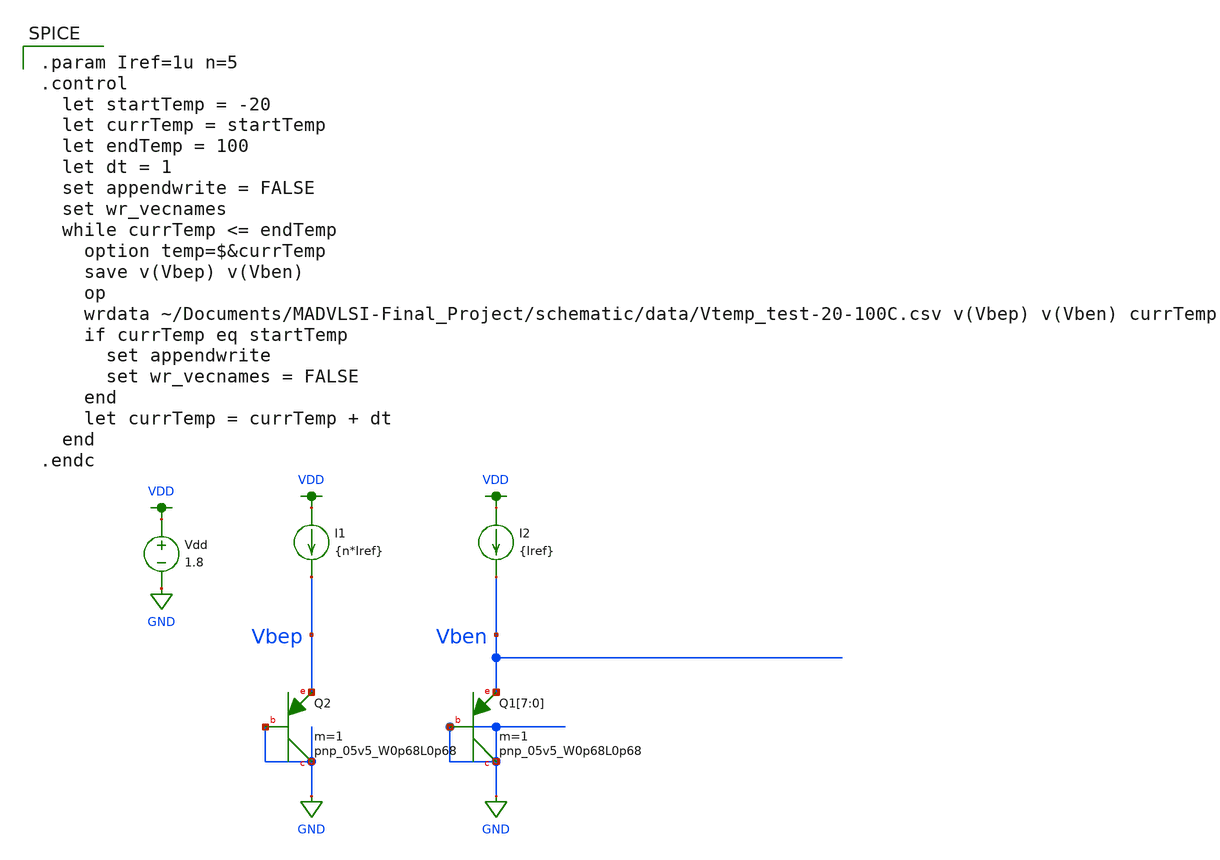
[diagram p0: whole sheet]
** sch_path: schematic/test/Vtemp_test.sch
**.subckt Vtemp_test
XQ2 GND GND Vbep sky130_fd_pr__pnp_05v5_W0p68L0p68 m=1
XQ1[7] GND GND Vben sky130_fd_pr__pnp_05v5_W0p68L0p68 m=1
XQ1[6] GND GND Vben sky130_fd_pr__pnp_05v5_W0p68L0p68 m=1
XQ1[5] GND GND Vben sky130_fd_pr__pnp_05v5_W0p68L0p68 m=1
XQ1[4] GND GND Vben sky130_fd_pr__pnp_05v5_W0p68L0p68 m=1
XQ1[3] GND GND Vben sky130_fd_pr__pnp_05v5_W0p68L0p68 m=1
XQ1[2] GND GND Vben sky130_fd_pr__pnp_05v5_W0p68L0p68 m=1
XQ1[1] GND GND Vben sky130_fd_pr__pnp_05v5_W0p68L0p68 m=1
XQ1[0] GND GND Vben sky130_fd_pr__pnp_05v5_W0p68L0p68 m=1
I1 VDD Vbep {n*Iref}
I2 VDD Vben {Iref}
Vdd VDD GND 1.8
**** begin user architecture code

.option wnflag=1
.param MC_SWITCH=0.0
.lib ~/skywater/skywater-pdk/libraries/sky130_fd_pr_ngspice/latest/models/sky130.lib.spice tt


.param Iref=1u n=5
.control
  let startTemp = -20
  let currTemp = startTemp
  let endTemp = 100
  let dt = 1
  set appendwrite = FALSE
  set wr_vecnames
  while currTemp <= endTemp
    option temp=$&currTemp
    save v(Vbep) v(Vben)
    op
    wrdata ~/Documents/MADVLSI-Final_Project/schematic/data/Vtemp_test-20-100C.csv v(Vbep) v(Vben)
+ currTemp
    if currTemp eq startTemp
      set appendwrite
      set wr_vecnames = FALSE
    end
    let currTemp = currTemp + dt
  end
.endc

**** end user architecture code
**.ends
.GLOBAL GND
.GLOBAL VDD
.end
